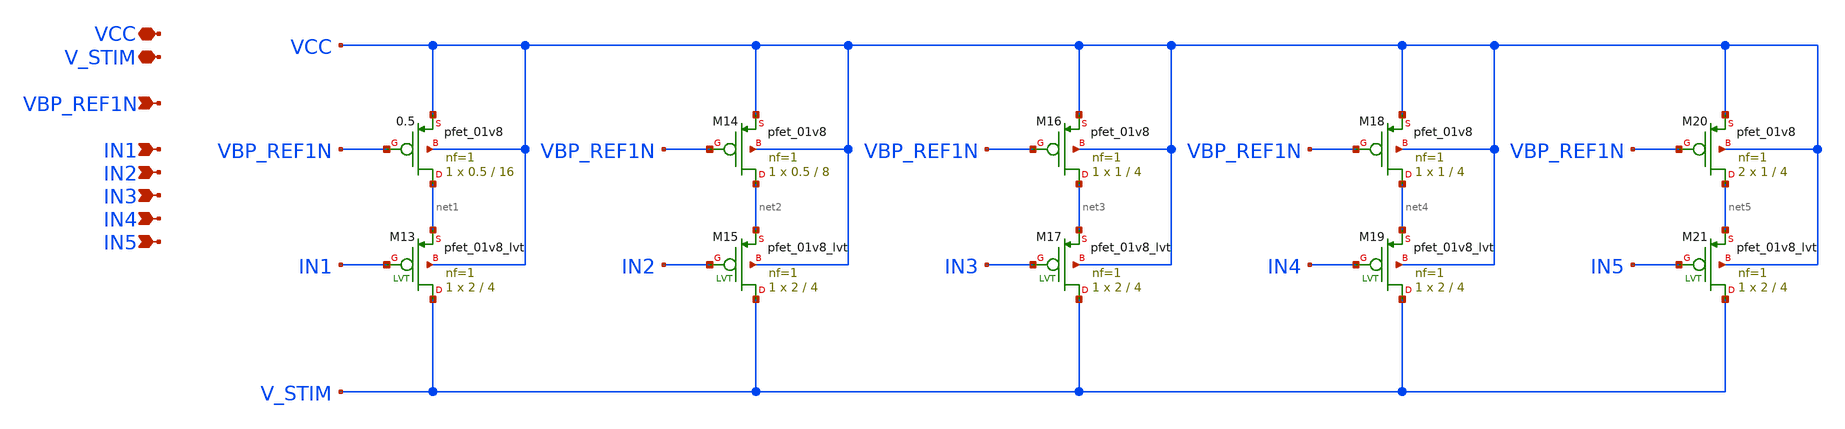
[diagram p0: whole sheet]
** sch_path: schem/input_current_bank.sch
**.subckt input_current_bank VCC V_STIM VBP_REF1N IN1 IN2 IN3 IN4 IN5
*.iopin VCC
*.iopin V_STIM
*.ipin VBP_REF1N
*.ipin IN1
*.ipin IN2
*.ipin IN3
*.ipin IN4
*.ipin IN5
X0.5 net1 VBP_REF1N VCC VCC sky130_fd_pr__pfet_01v8 L=16 W=0.5 nf=1 ad='int((1 + 1)/2) * 0.5 / 1 * 0.29'
+ as='int((1 + 2)/2) * 0.5 / 1 * 0.29' pd='2*int((1 + 1)/2) * (0.5 / 1 + 0.29)' ps='2*int((1 + 2)/2) * (0.5 / 1 + 0.29)'
+ nrd='0.29 / 0.5 ' nrs='0.29 / 0.5 ' sa=0 sb=0 sd=0 mult=1 m=1
XM13 V_STIM IN1 net1 VCC sky130_fd_pr__pfet_01v8_lvt L=4 W=2 nf=1 ad='int((1 + 1)/2) * 2 / 1 * 0.29'
+ as='int((1 + 2)/2) * 2 / 1 * 0.29' pd='2*int((1 + 1)/2) * (2 / 1 + 0.29)' ps='2*int((1 + 2)/2) * (2 / 1 + 0.29)'
+ nrd='0.29 / 2 ' nrs='0.29 / 2 ' sa=0 sb=0 sd=0 mult=1 m=1
XM14 net2 VBP_REF1N VCC VCC sky130_fd_pr__pfet_01v8 L=8 W=0.5 nf=1 ad='int((1 + 1)/2) * 0.5 / 1 * 0.29'
+ as='int((1 + 2)/2) * 0.5 / 1 * 0.29' pd='2*int((1 + 1)/2) * (0.5 / 1 + 0.29)' ps='2*int((1 + 2)/2) * (0.5 / 1 + 0.29)'
+ nrd='0.29 / 0.5 ' nrs='0.29 / 0.5 ' sa=0 sb=0 sd=0 mult=1 m=1
XM15 V_STIM IN2 net2 VCC sky130_fd_pr__pfet_01v8_lvt L=4 W=2 nf=1 ad='int((1 + 1)/2) * 2 / 1 * 0.29'
+ as='int((1 + 2)/2) * 2 / 1 * 0.29' pd='2*int((1 + 1)/2) * (2 / 1 + 0.29)' ps='2*int((1 + 2)/2) * (2 / 1 + 0.29)'
+ nrd='0.29 / 2 ' nrs='0.29 / 2 ' sa=0 sb=0 sd=0 mult=1 m=1
XM16 net3 VBP_REF1N VCC VCC sky130_fd_pr__pfet_01v8 L=4 W=1 nf=1 ad='int((1 + 1)/2) * 1 / 1 * 0.29' as='int((1 + 2)/2) * 1 / 1 * 0.29'
+ pd='2*int((1 + 1)/2) * (1 / 1 + 0.29)' ps='2*int((1 + 2)/2) * (1 / 1 + 0.29)' nrd='0.29 / 1 ' nrs='0.29 / 1 '
+ sa=0 sb=0 sd=0 mult=1 m=1
XM17 V_STIM IN3 net3 VCC sky130_fd_pr__pfet_01v8_lvt L=4 W=2 nf=1 ad='int((1 + 1)/2) * 2 / 1 * 0.29'
+ as='int((1 + 2)/2) * 2 / 1 * 0.29' pd='2*int((1 + 1)/2) * (2 / 1 + 0.29)' ps='2*int((1 + 2)/2) * (2 / 1 + 0.29)'
+ nrd='0.29 / 2 ' nrs='0.29 / 2 ' sa=0 sb=0 sd=0 mult=1 m=1
XM18 net4 VBP_REF1N VCC VCC sky130_fd_pr__pfet_01v8 L=4 W=1 nf=1 ad='int((1 + 1)/2) * 1 / 1 * 0.29' as='int((1 + 2)/2) * 1 / 1 * 0.29'
+ pd='2*int((1 + 1)/2) * (1 / 1 + 0.29)' ps='2*int((1 + 2)/2) * (1 / 1 + 0.29)' nrd='0.29 / 1 ' nrs='0.29 / 1 '
+ sa=0 sb=0 sd=0 mult=1 m=1
XM19 V_STIM IN4 net4 VCC sky130_fd_pr__pfet_01v8_lvt L=4 W=2 nf=1 ad='int((1 + 1)/2) * 2 / 1 * 0.29'
+ as='int((1 + 2)/2) * 2 / 1 * 0.29' pd='2*int((1 + 1)/2) * (2 / 1 + 0.29)' ps='2*int((1 + 2)/2) * (2 / 1 + 0.29)'
+ nrd='0.29 / 2 ' nrs='0.29 / 2 ' sa=0 sb=0 sd=0 mult=1 m=1
XM20 net5 VBP_REF1N VCC VCC sky130_fd_pr__pfet_01v8 L=4 W=1 nf=1 ad='int((1 + 1)/2) * 1 / 1 * 0.29' as='int((1 + 2)/2) * 1 / 1 * 0.29'
+ pd='2*int((1 + 1)/2) * (1 / 1 + 0.29)' ps='2*int((1 + 2)/2) * (1 / 1 + 0.29)' nrd='0.29 / 1 ' nrs='0.29 / 1 '
+ sa=0 sb=0 sd=0 mult=2 m=2
XM21 V_STIM IN5 net5 VCC sky130_fd_pr__pfet_01v8_lvt L=4 W=2 nf=1 ad='int((1 + 1)/2) * 2 / 1 * 0.29'
+ as='int((1 + 2)/2) * 2 / 1 * 0.29' pd='2*int((1 + 1)/2) * (2 / 1 + 0.29)' ps='2*int((1 + 2)/2) * (2 / 1 + 0.29)'
+ nrd='0.29 / 2 ' nrs='0.29 / 2 ' sa=0 sb=0 sd=0 mult=1 m=1
**.ends
.end
